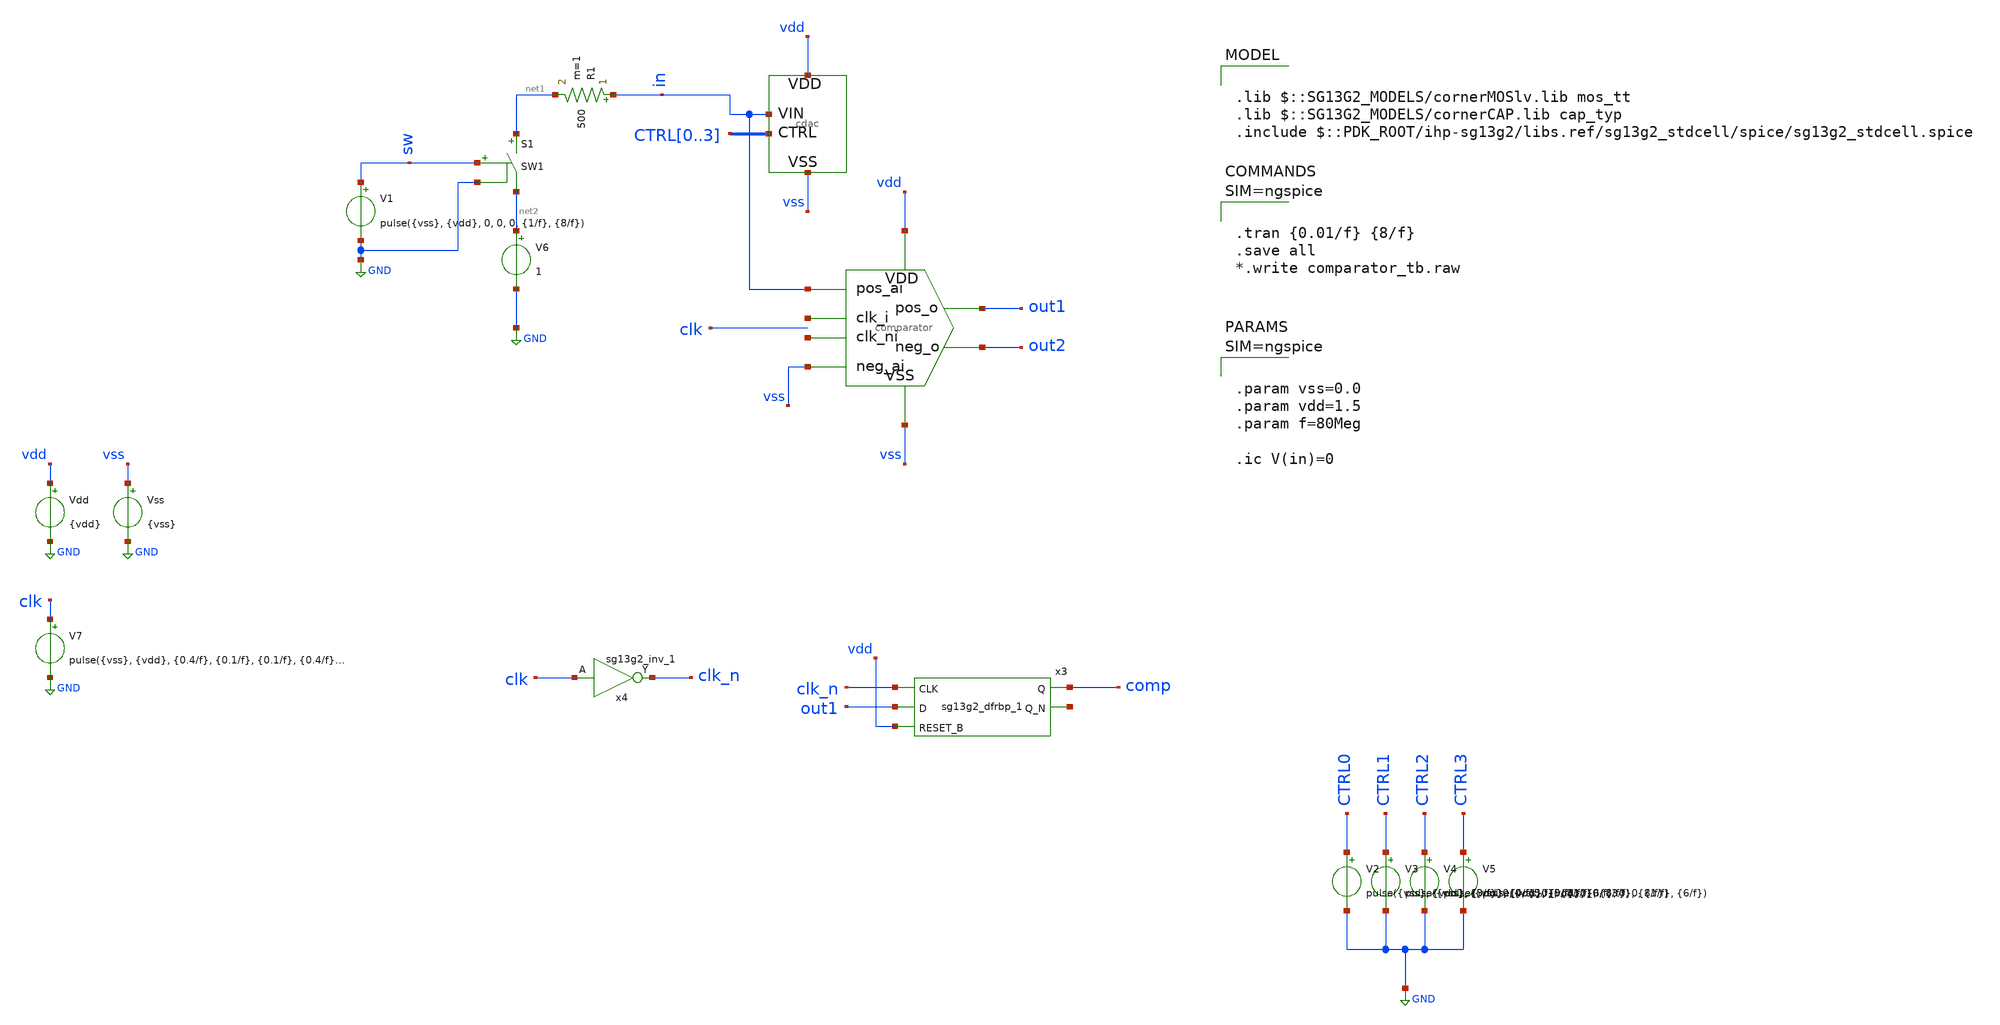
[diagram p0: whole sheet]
** sch_path: designs/cdac/cdac_tb.sch
**.subckt cdac_tb
x1 in CTRL0 CTRL1 CTRL2 CTRL3 vss vdd cdac
S1 net1 net2 sw GND SW1
R1 in net1 500 m=1
V1 sw GND pulse({vss}, {vdd}, 0, 0, 0, {1/f}, {8/f})
Vdd vdd GND {vdd}
Vss vss GND {vss}
V2 CTRL0 GND pulse({vss}, {vdd}, {3/f}, 0, 0, {5/f}, {8/f})
V3 CTRL1 GND pulse({vss}, {vdd}, {4/f}, 0, 0, {1/f}, {8/f})
V4 CTRL2 GND pulse({vss}, {vdd}, {5/f}, 0, 0, {3/f}, {8/f})
V5 CTRL3 GND pulse({vss}, {vdd}, {6/f}, 0, 0, {1/f}, {6/f})
V6 net2 GND 1
x2 net3 in vss out2 out1 vss vdd net4 comparator
V7 clk GND pulse({vss}, {vdd}, {0.4/f}, {0.1/f}, {0.1/f}, {0.4/f}, {1/f})
x4 clk_n clk VDD VSS sg13g2_inv_1
x3 comp net5 clk_n out1 vdd VDD VSS sg13g2_dfrbp_1
**** begin user architecture code

.lib $::SG13G2_MODELS/cornerMOSlv.lib mos_tt
.lib $::SG13G2_MODELS/cornerCAP.lib cap_typ
.include $::PDK_ROOT/ihp-sg13g2/libs.ref/sg13g2_stdcell/spice/sg13g2_stdcell.spice




.tran {0.01/f} {8/f}
.save all
*.write comparator_tb.raw






.param vss=0.0
.param vdd=1.5
.param f=80Meg

.ic V(in)=0



**** end user architecture code
**.ends

* expanding   symbol:  cdac.sym # of pins=4
** sym_path: designs/cdac/cdac.sym
** sch_path: designs/cdac/cdac.sch
.subckt cdac VIN CTRL0 CTRL1 CTRL2 CTRL3 VSS VDD
*.ipin VSS
*.ipin VIN
*.ipin CTRL0,CTRL1,CTRL2,CTRL3
*.ipin VDD
XC1 VIN l1 cap_cmim w=2.577e-5 l=2.577e-5 m=1 mm_ok=1
XC2 VIN l2 cap_cmim w=1.820e-5 l=1.820e-5 m=1 mm_ok=1
XC3 VIN l3 cap_cmim w=1.286e-5 l=1.286e-5 m=1 mm_ok=1
XC4 VIN l4 cap_cmim w=9.076e-6 l=9.076e-6 m=1 mm_ok=1
x1 l1 CTRL0 VDD VSS sg13g2_inv_1
x2 l2 CTRL1 VDD VSS sg13g2_inv_1
x3 l3 CTRL2 VDD VSS sg13g2_inv_1
x4 l4 CTRL3 VDD VSS sg13g2_inv_1
XC5 VIN VSS cap_cmim w=9.076e-6 l=9.076e-6 m=1 mm_ok=1
.ends


* expanding   symbol:  /workspaces/ngspice_cosim_inv/designs/comparator/comparator.sym # of pins=8
** sym_path: designs/comparator_dt/comparator.sym
** sch_path: designs/comparator_dt/comparator.sch
.subckt comparator clk_i pos_ai neg_ai neg_o pos_o VSS VDD clk_ni
*.ipin pos_ai
*.ipin neg_ai
*.ipin VSS
*.ipin VDD
*.opin neg_o
*.opin pos_o
*.ipin clk_i
*.ipin clk_ni
XM12 neg_buf clk_i VDD VDD sg13_lv_pmos w=1.0u l=0.13u ng=1 m=1 mm_ok=1
XM13 pos_buf clk_i VDD VDD sg13_lv_pmos w=1.0u l=0.13u ng=1 m=1 mm_ok=1
XM14 net1 pos_ai neg_buf VSS sg13_lv_nmos w=1.0u l=0.13u ng=1 m=1 mm_ok=1
XM15 net1 neg_ai pos_buf VSS sg13_lv_nmos w=1.0u l=0.13u ng=1 m=1 mm_ok=1
XM16 VSS clk_i net1 VSS sg13_lv_nmos w=1.0u l=0.13u ng=1 m=1 mm_ok=1
XM17 net2 clk_ni VDD VDD sg13_lv_pmos w=2.0u l=0.13u ng=2 m=1 mm_ok=1
XM18 pos_o neg_o net2 VDD sg13_lv_pmos w=2.0u l=0.13u ng=2 m=1 mm_ok=1
XM19 neg_o pos_o net2 VDD sg13_lv_pmos w=2.0u l=0.13u ng=2 m=1 mm_ok=1
XM20 VSS neg_buf pos_o VSS sg13_lv_nmos w=1.0u l=0.13u ng=1 m=1 mm_ok=1
XM21 VSS neg_o pos_o VSS sg13_lv_nmos w=1.0u l=0.13u ng=1 m=1 mm_ok=1
XM22 VSS pos_o neg_o VSS sg13_lv_nmos w=1.0u l=0.13u ng=1 m=1 mm_ok=1
XM23 VSS pos_buf neg_o VSS sg13_lv_nmos w=1.0u l=0.13u ng=1 m=1 mm_ok=1
XC1 neg_buf VSS cap_cmim w=1.41e-5 l=1.41e-5 m=1 mm_ok=1
XC2 pos_buf VSS cap_cmim w=1.41e-5 l=1.41e-5 m=1 mm_ok=1
.ends


* expanding   symbol:  sg13g2_stdcells/sg13g2_inv_1.sym # of pins=2
** sym_path: sg13g2_stdcells/sg13g2_inv_1.sym
** sch_path: sg13g2_stdcells/sg13g2_inv_1.sch
.subckt sg13g2_inv_1 Y A VDD VSS
*.opin Y
*.ipin A
*.iopin VDD
*.iopin VSS
XM1 Y A VSS VSS sg13_lv_nmos w=740.00n l=130.00n ng=1 m=1 mm_ok=1
XM2 Y A VDD VDD sg13_lv_pmos w=1.12u l=130.00n ng=1 m=1 mm_ok=1
.ends


* expanding   symbol:  sg13g2_stdcells/sg13g2_dfrbp_1.sym # of pins=5
** sym_path: sg13g2_stdcells/sg13g2_dfrbp_1.sym
** sch_path: sg13g2_stdcells/sg13g2_dfrbp_1.sch
.subckt sg13g2_dfrbp_1 Q Q_N CLK D RESET_B VDD VSS
*.ipin D
*.ipin RESET_B
*.ipin CLK
*.opin Q
*.opin Q_N
*.iopin VDD
*.iopin VSS
XM1 Db D net10 VSS sg13_lv_nmos w=420.00n l=130.00n ng=1 m=1 mm_ok=1
XM2 net10 RESET_B VSS VSS sg13_lv_nmos w=420.00n l=130.00n ng=1 m=1 mm_ok=1
XM3 net1 clkneg net9 VSS sg13_lv_nmos w=420.00n l=130.00n ng=1 m=1 mm_ok=1
XM4 net9 net1 VSS VSS sg13_lv_nmos w=420.00n l=130.00n ng=1 m=1 mm_ok=1
XM5 net1 net1 net5 VSS sg13_lv_nmos w=420.00n l=130.00n ng=1 m=1 mm_ok=1
XM6 net5 RESET_B VSS VSS sg13_lv_nmos w=420.00n l=130.00n ng=1 m=1 mm_ok=1
XM7 Q_N net1 VSS VSS sg13_lv_nmos w=740.00n l=130.00n ng=1 m=1 mm_ok=1
XM8 net2 net1 VSS VSS sg13_lv_nmos w=740.00n l=130.00n ng=1 m=1 mm_ok=1
XM9 Q net2 VSS VSS sg13_lv_nmos w=740.00n l=130.00n ng=1 m=1 mm_ok=1
XM10 clkneg CLK VSS VSS sg13_lv_nmos w=740.00n l=130.00n ng=1 m=1 mm_ok=1
XM11 clkpos clkneg VSS VSS sg13_lv_nmos w=740.00n l=130.00n ng=1 m=1 mm_ok=1
XM12 Db clkneg net3 VSS sg13_lv_nmos w=420.00n l=130.00n ng=1 m=1 mm_ok=1
XM13 net3 clkpos net8 VSS sg13_lv_nmos w=420.00n l=130.00n ng=1 m=1 mm_ok=1
XM14 net8 net3 net4 VSS sg13_lv_nmos w=420.00n l=130.00n ng=1 m=1 mm_ok=1
XM15 net4 RESET_B VSS VSS sg13_lv_nmos w=420.00n l=130.00n ng=1 m=1 mm_ok=1
XM16 net3 net3 VSS VSS sg13_lv_nmos w=740.00n l=130.00n ng=1 m=1 mm_ok=1
XM17 net3 clkpos net1 VSS sg13_lv_nmos w=740.00n l=130.00n ng=1 m=1 mm_ok=1
XM18 Db RESET_B VDD VDD sg13_lv_pmos w=420.00n l=130.00n ng=1 m=1 mm_ok=1
XM19 Db D VDD VDD sg13_lv_pmos w=420.00n l=130.00n ng=1 m=1 mm_ok=1
XM20 net7 net1 VDD VDD sg13_lv_pmos w=420.00n l=130.00n ng=1 m=1 mm_ok=1
XM21 net1 clkpos net7 VDD sg13_lv_pmos w=420.00n l=130.00n ng=1 m=1 mm_ok=1
XM22 net1 net1 VDD VDD sg13_lv_pmos w=420.00n l=130.00n ng=1 m=1 mm_ok=1
XM23 net1 RESET_B VDD VDD sg13_lv_pmos w=420.00n l=130.00n ng=1 m=1 mm_ok=1
XM24 Q_N net1 VDD VDD sg13_lv_pmos w=1.12u l=130.00n ng=1 m=1 mm_ok=1
XM25 net2 net1 VDD VDD sg13_lv_pmos w=1.12u l=130.00n ng=1 m=1 mm_ok=1
XM26 Q net2 VDD VDD sg13_lv_pmos w=1.12u l=130.00n ng=1 m=1 mm_ok=1
XM27 clkneg CLK VDD VDD sg13_lv_pmos w=1.12u l=130.00n ng=1 m=1 mm_ok=1
XM28 clkpos clkneg VDD VDD sg13_lv_pmos w=1.12u l=130.00n ng=1 m=1 mm_ok=1
XM29 Db clkpos net3 VDD sg13_lv_pmos w=420.00n l=130.00n ng=1 m=1 mm_ok=1
XM30 net6 net3 VDD VDD sg13_lv_pmos w=420.00n l=130.00n ng=1 m=1 mm_ok=1
XM31 net3 clkneg net6 VDD sg13_lv_pmos w=420.00n l=130.00n ng=1 m=1 mm_ok=1
XM32 net3 RESET_B VDD VDD sg13_lv_pmos w=420.00n l=130.00n ng=1 m=1 mm_ok=1
XM33 net3 net3 VDD VDD sg13_lv_pmos w=1.000u l=130.00n ng=1 m=1 mm_ok=1
XM34 net3 clkneg net1 VDD sg13_lv_pmos w=1.000u l=130.00n ng=1 m=1 mm_ok=1
.ends

.GLOBAL GND
**** begin user architecture code
.MODEL SW1 SW   VT=0.9 VH=0.01  RON=0.01 ROFF=10G
**** end user architecture code
.end
